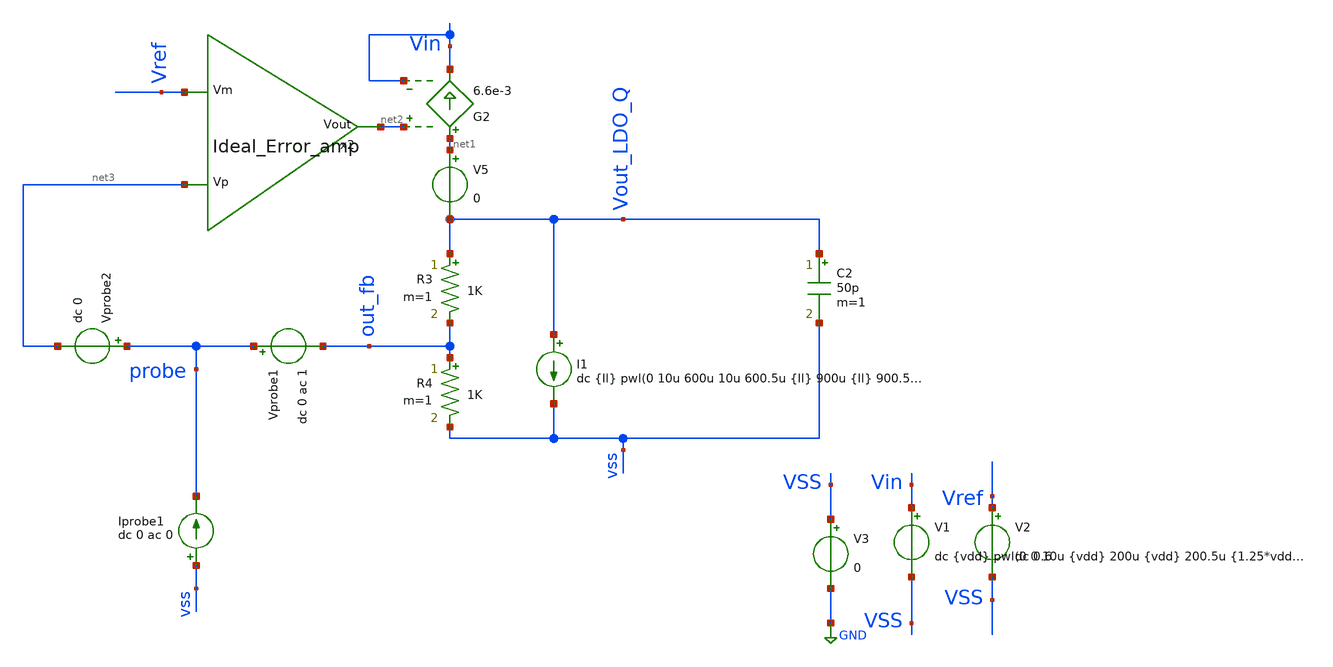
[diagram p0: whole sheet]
** sch_path: EE_628_LDO/LDO_STB_Tian_mbrook.sch
* EE_628_LDO/Ideal_Error_amp.sch:
* Copyright 2023 IHP PDK Authors
**.subckt LDO_STB_Tian_mbrook
I1 Vout_LDO_Q vss dc {Il} pwl(0 10u 600u 10u 600.5u {Il} 900u {Il} 900.5u 10u)
C2 Vout_LDO_Q vss 50p m=1
G2 net1 Vin net2 Vin 6.6e-3
V5 net1 Vout_LDO_Q 0
x2 net2 Vref net3 Ideal_Error_amp
R3 Vout_LDO_Q out_fb 1K m=1
R4 out_fb vss 1K m=1
V2 Vref VSS dc 0.6
V3 VSS GND 0
V1 Vin VSS dc {vdd} pwl(0 0 10u {vdd} 200u {vdd} 200.5u {1.25*vdd} 500u {1.25*vdd} 500.5u {vdd})
Iprobe1 vss probe dc 0 ac 0
Vprobe1 probe out_fb dc 0 ac 1
Vprobe2 probe net3 dc 0
**** begin user architecture code
 * Model Corners
.lib /foss/pdks/sg13g2/libs.tech/ngspice/models/cornerMOSlv.lib mos_tt
.lib /foss/pdks/sg13g2/libs.tech/ngspice/models/cornerRES.lib res_typ





.param B=0 temp=27 vdd=1.8 Il=2m Res=1Meg Cap=10p Gm=20m
**.model mysw SW vt={vdd/2} ron=10k roff=10gig reltol=1e-4

.control
save all



************************************ Test ************

.OPTIONS itl1=200
.OPTIONS itl2=200
.OPTIONS itl4=200

let runs=2
let run=0

alter @Vprobe1[acmag]=1
alter @Iprobe1[acmag]=0

dowhile run<runs
set run =$&run
set temp=27

ac dec 20 0.01 500meg
**write LDO_testLDO_stb_tb_{$run}.raw

**all

alter @Vprobe1[acmag]=0
alter @Iprobe1[acmag]=1

let run=run + 1

end

let ip11 = ac1.i(Vprobe1)
let ip12 = ac1.i(Vprobe2)
let ip21 = ac2.i(Vprobe1)
let ip22 = ac2.i(Vprobe2)
let vprb1 = ac1.v(probe)
let vprb2 = ac2.v(probe)

let mb = 1/(vprb1+ip22)-1

let av = 1/(1/(2*(ip11*vprb2-vprb1*ip21)+vprb1+ip21)-1)

let phase=180/PI*vp(av)
let phase_mb = 180/PI*vp(mb)
plot vdb(av)
plot phase
plot vdb(mb)
plot phase_mb
plot vdb(mb) phase_mb xlog
plot vdb(av) phase xlog

echo “—-”
echo “—-”

meas ac gm_db find vdb(av) when vp(av)=0
meas ac pm_deg find phase when vdb(av)=0
meas ac 3db_f when phase=135
meas ac 0db_f when vdb(av)=0
meas ac dc_gain find vdb(av) at=0.01
meas ac m6dB when vdB(av)=-6

echo “—-”
echo “—-”



.endc

**** end user architecture code
**.ends

* expanding   symbol:  /foss/designs/EE628_LDO/Ideal_Error_amp.sym # of pins=3
** sym_path: EE_628_LDO/Ideal_Error_amp.sym
** sch_path: EE_628_LDO/Ideal_Error_amp.sch
.subckt Ideal_Error_amp Vout Vm Vp
*.ipin Vm
*.ipin Vp
*.opin Vout
E1 Vout GND net1 GND 1
**** begin user architecture code

.lib /foss/pdks/sg13g2/libs.tech/ngspice/models/cornerMOSlv.lib mos_tt
.lib /foss/pdks/sg13g2/libs.tech/ngspice/models/cornerRES.lib res_typ
**.lib /foss/pdks/sg13g2/libs.tech/ngspice/models/sg13g2_moslv_mod.lib mos_tt
**.lib /foss/pdks/sg13g2/libs.tech/ngspice/models/sg13g2_moslv_parm.lib mos_tt
**.lib /foss/pdks/sg13g2/libs.tech/ngspice/models/sg13g2_moslv_stat.lib mos_tt

**** end user architecture code
G1 GND net1 Vp Vm Gm
R1 net1 GND Res m=1
C1 net1 GND Cap m=1
V2 net2 GND dc 0.7 ac 1
V1 net3 GND dc 0.7
.ends

.GLOBAL GND
.end
